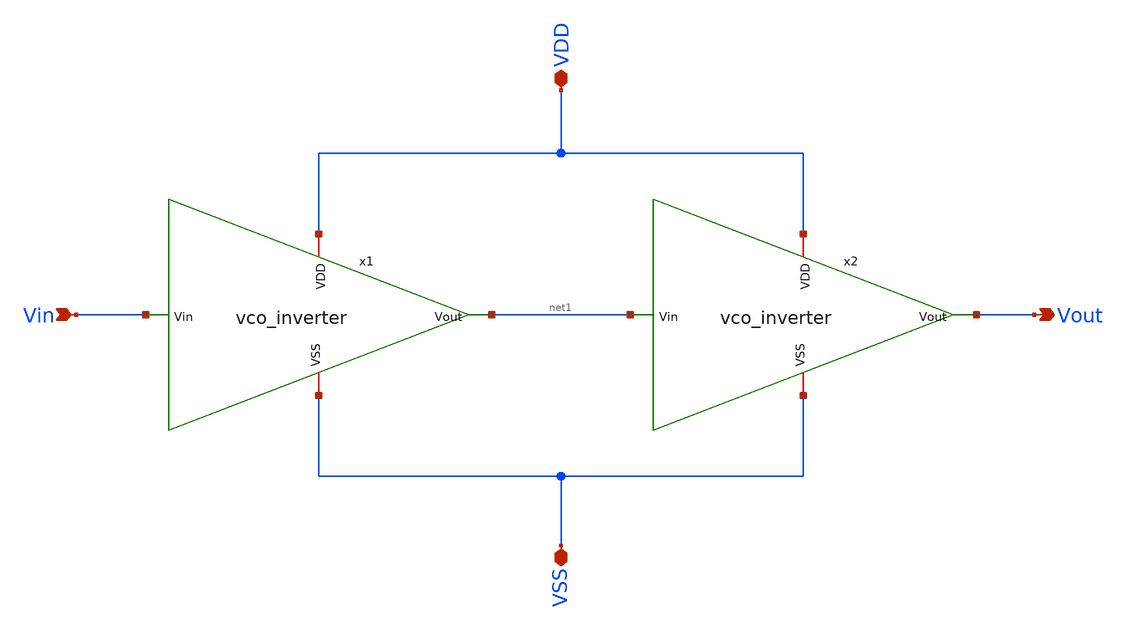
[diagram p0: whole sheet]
** sch_path: xschem/vco_buffer.sch
**.subckt vco_buffer VDD VSS Vin Vout
*.iopin VDD
*.iopin VSS
*.ipin Vin
*.opin Vout
x1 VDD Vin net1 VSS vco_inverter
x2 VDD net1 Vout VSS vco_inverter
**.ends

* expanding   symbol:  vco_inverter.sym # of pins=4
** sym_path: xschem/vco_inverter.sym
** sch_path: xschem/vco_inverter.sch
.subckt vco_inverter VDD Vin Vout VSS
*.iopin VDD
*.iopin VSS
*.ipin Vin
*.opin Vout
XM1 Vout Vin VSS VSS sky130_fd_pr__nfet_01v8 L=0.15 W=1 nf=1 ad='int((nf+1)/2) * W/nf * 0.29' as='int((nf+2)/2) * W/nf * 0.29'
+ pd='2*int((nf+1)/2) * (W/nf + 0.29)' ps='2*int((nf+2)/2) * (W/nf + 0.29)' nrd='0.29 / W' nrs='0.29 / W'
+ sa=0 sb=0 sd=0 mult=1 m=1
XM2 Vout Vin VDD VDD sky130_fd_pr__pfet_01v8 L=0.15 W=1 nf=1 ad='int((nf+1)/2) * W/nf * 0.29' as='int((nf+2)/2) * W/nf * 0.29'
+ pd='2*int((nf+1)/2) * (W/nf + 0.29)' ps='2*int((nf+2)/2) * (W/nf + 0.29)' nrd='0.29 / W' nrs='0.29 / W'
+ sa=0 sb=0 sd=0 mult=1 m=1
.ends

.end
